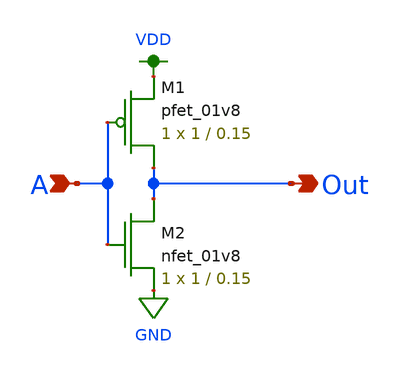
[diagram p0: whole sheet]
** sch_path: miniproject2/MP1_inverter.sch
**.subckt MP1_inverter A Out
*.ipin A
*.opin Out
XM1 Out A VDD VDD sky130_fd_pr__pfet_01v8 L=0.15 W=1 nf=1 ad='int((nf+1)/2) * W/nf * 0.29' as='int((nf+2)/2) * W/nf * 0.29'
+ pd='2*int((nf+1)/2) * (W/nf + 0.29)' ps='2*int((nf+2)/2) * (W/nf + 0.29)' nrd='0.29 / W' nrs='0.29 / W'
+ sa=0 sb=0 sd=0 mult=1 m=1
XM2 Out A GND GND sky130_fd_pr__nfet_01v8 L=0.15 W=1 nf=1 ad='int((nf+1)/2) * W/nf * 0.29' as='int((nf+2)/2) * W/nf * 0.29'
+ pd='2*int((nf+1)/2) * (W/nf + 0.29)' ps='2*int((nf+2)/2) * (W/nf + 0.29)' nrd='0.29 / W' nrs='0.29 / W'
+ sa=0 sb=0 sd=0 mult=1 m=1
**.ends
.GLOBAL VDD
.GLOBAL GND
.end
